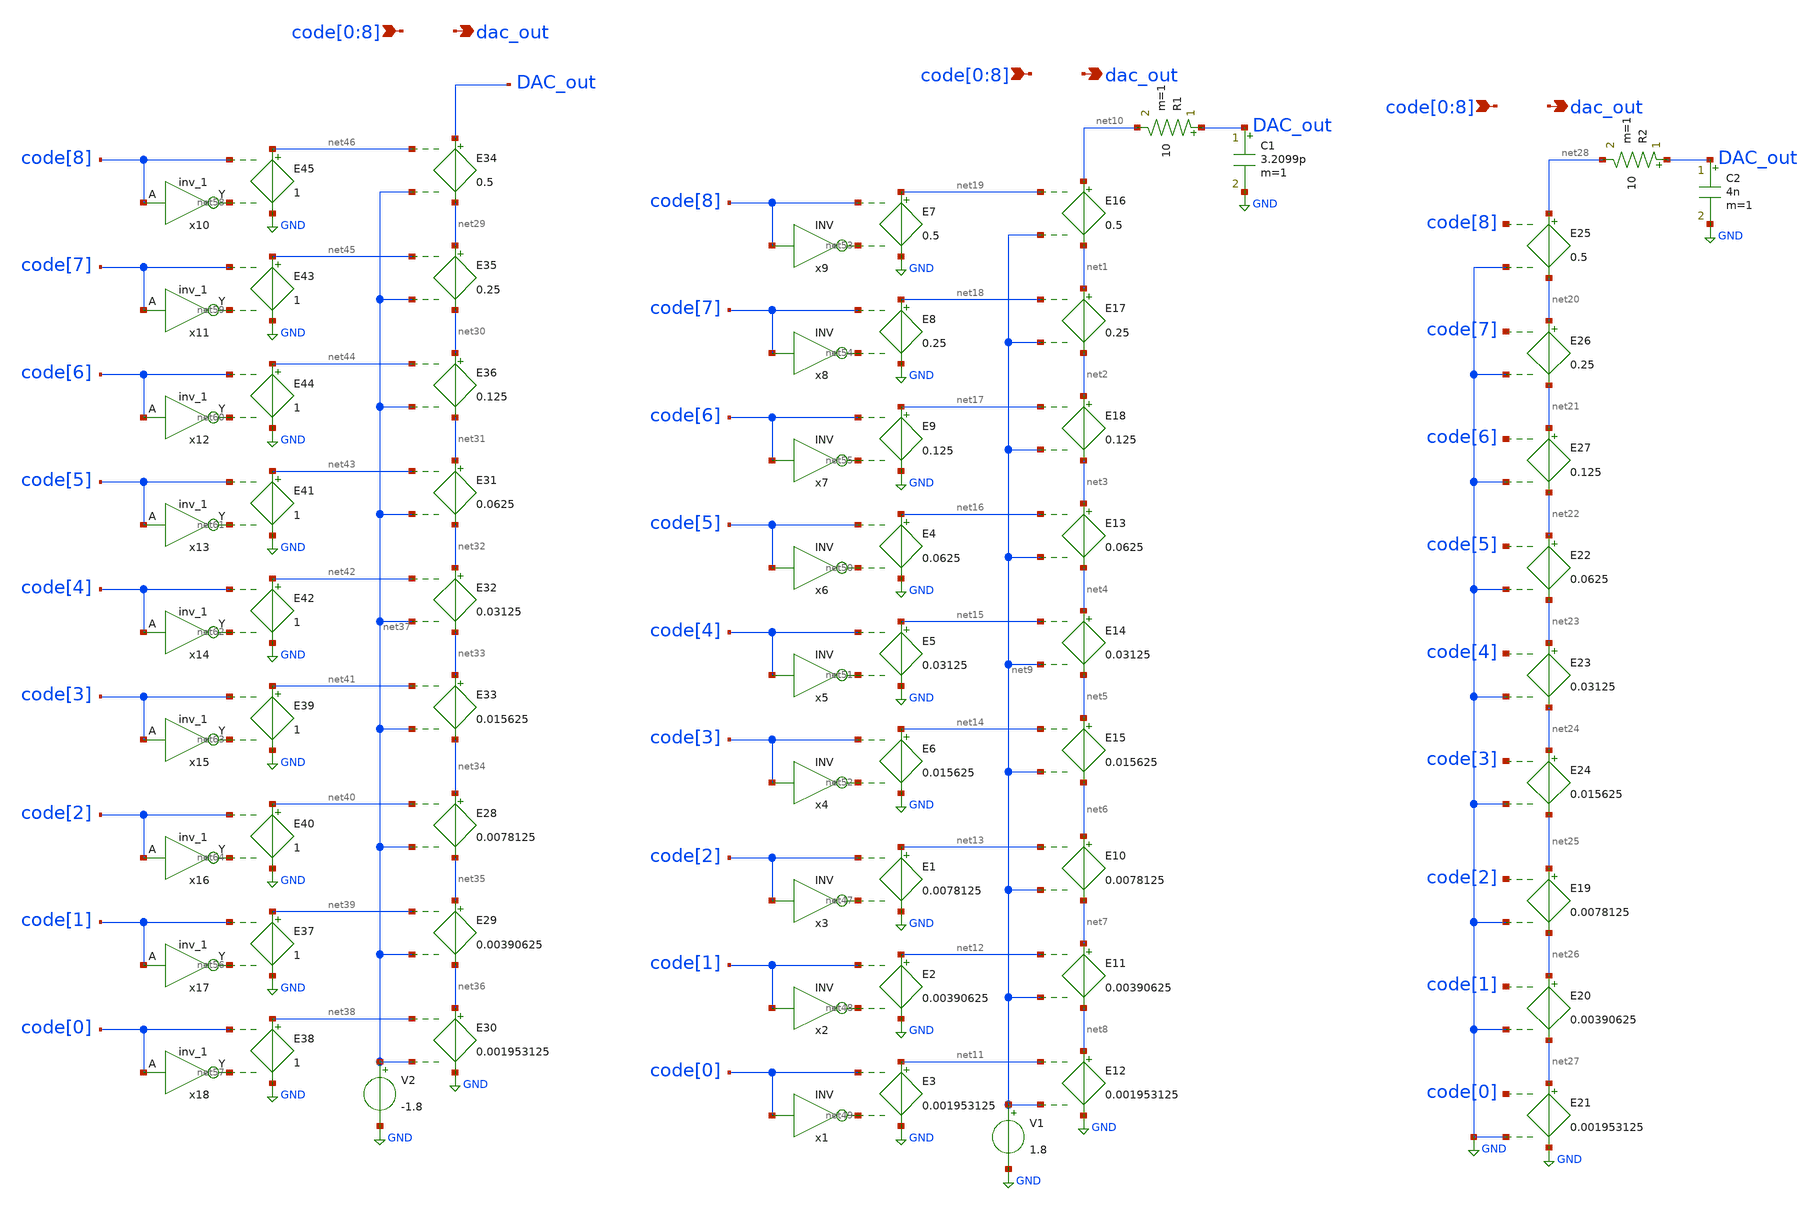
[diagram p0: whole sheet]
** sch_path: tb/ideal_dac.sch
**.subckt ideal_dac code[0],code[1],code[2],code[3],code[4],code[5],code[6],code[7],code[8] dac_out
*+ code[0],code[1],code[2],code[3],code[4],code[5],code[6],code[7],code[8] dac_out code[0],code[1],code[2],code[3],code[4],code[5],code[6],code[7],code[8] dac_out
*.ipin code[0],code[1],code[2],code[3],code[4],code[5],code[6],code[7],code[8]
*.opin dac_out
*.ipin code[0],code[1],code[2],code[3],code[4],code[5],code[6],code[7],code[8]
*.opin dac_out
*.ipin code[0],code[1],code[2],code[3],code[4],code[5],code[6],code[7],code[8]
*.opin dac_out
E10 net6 net7 net13 net9 0.0078125
E11 net7 net8 net12 net9 0.00390625
E12 net8 GND net11 net9 0.001953125
E13 net3 net4 net16 net9 0.0625
E14 net4 net5 net15 net9 0.03125
E15 net5 net6 net14 net9 0.015625
E16 net10 net1 net19 net9 0.5
E17 net1 net2 net18 net9 0.25
E18 net2 net3 net17 net9 0.125
E1 net13 GND code[2] net47 0.0078125
E2 net12 GND code[1] net48 0.00390625
E3 net11 GND code[0] net49 0.001953125
E4 net16 GND code[5] net50 0.0625
E5 net15 GND code[4] net51 0.03125
E6 net14 GND code[3] net52 0.015625
E7 net19 GND code[8] net53 0.5
E8 net18 GND code[7] net54 0.25
E9 net17 GND code[6] net55 0.125
V1 net9 GND 1.8
x1 net49 code[0] VCC VSS VCC VSS INV
x2 net48 code[1] VCC VSS VCC VSS INV
x3 net47 code[2] VCC VSS VCC VSS INV
x4 net52 code[3] VCC VSS VCC VSS INV
x5 net51 code[4] VCC VSS VCC VSS INV
x6 net50 code[5] VCC VSS VCC VSS INV
x7 net55 code[6] VCC VSS VCC VSS INV
x8 net54 code[7] VCC VSS VCC VSS INV
x9 net53 code[8] VCC VSS VCC VSS INV
C1 DAC_out GND 3.2099p m=1
R1 DAC_out net10 10 m=1
E19 net25 net26 code[2] GND 0.0078125
E20 net26 net27 code[1] GND 0.00390625
E21 net27 GND code[0] GND 0.001953125
E22 net22 net23 code[5] GND 0.0625
E23 net23 net24 code[4] GND 0.03125
E24 net24 net25 code[3] GND 0.015625
E25 net28 net20 code[8] GND 0.5
E26 net20 net21 code[7] GND 0.25
E27 net21 net22 code[6] GND 0.125
C2 DAC_out GND 4n m=1
R2 DAC_out net28 10 m=1
E28 net34 net35 net40 net37 0.0078125
E29 net35 net36 net39 net37 0.00390625
E30 net36 GND net38 net37 0.001953125
E31 net31 net32 net43 net37 0.0625
E32 net32 net33 net42 net37 0.03125
E33 net33 net34 net41 net37 0.015625
E34 DAC_out net29 net46 net37 0.5
E35 net29 net30 net45 net37 0.25
E36 net30 net31 net44 net37 0.125
E37 net39 GND code[1] net56 1
E38 net38 GND code[0] net57 1
V2 net37 GND -1.8
x10 code[8] VSS VSS VDD VDD net58 sky130_fd_sc_hd__inv_1
x11 code[7] VSS VSS VDD VDD net59 sky130_fd_sc_hd__inv_1
x12 code[6] VSS VSS VDD VDD net60 sky130_fd_sc_hd__inv_1
x13 code[5] VSS VSS VDD VDD net61 sky130_fd_sc_hd__inv_1
x14 code[4] VSS VSS VDD VDD net62 sky130_fd_sc_hd__inv_1
x15 code[3] VSS VSS VDD VDD net63 sky130_fd_sc_hd__inv_1
x16 code[2] VSS VSS VDD VDD net64 sky130_fd_sc_hd__inv_1
x17 code[1] VSS VSS VDD VDD net56 sky130_fd_sc_hd__inv_1
x18 code[0] VSS VSS VDD VDD net57 sky130_fd_sc_hd__inv_1
E39 net41 GND code[3] net63 1
E40 net40 GND code[2] net64 1
E41 net43 GND code[5] net61 1
E42 net42 GND code[4] net62 1
E43 net45 GND code[7] net59 1
E44 net44 GND code[6] net60 1
E45 net46 GND code[8] net58 1
**.ends
.GLOBAL GND
.end
